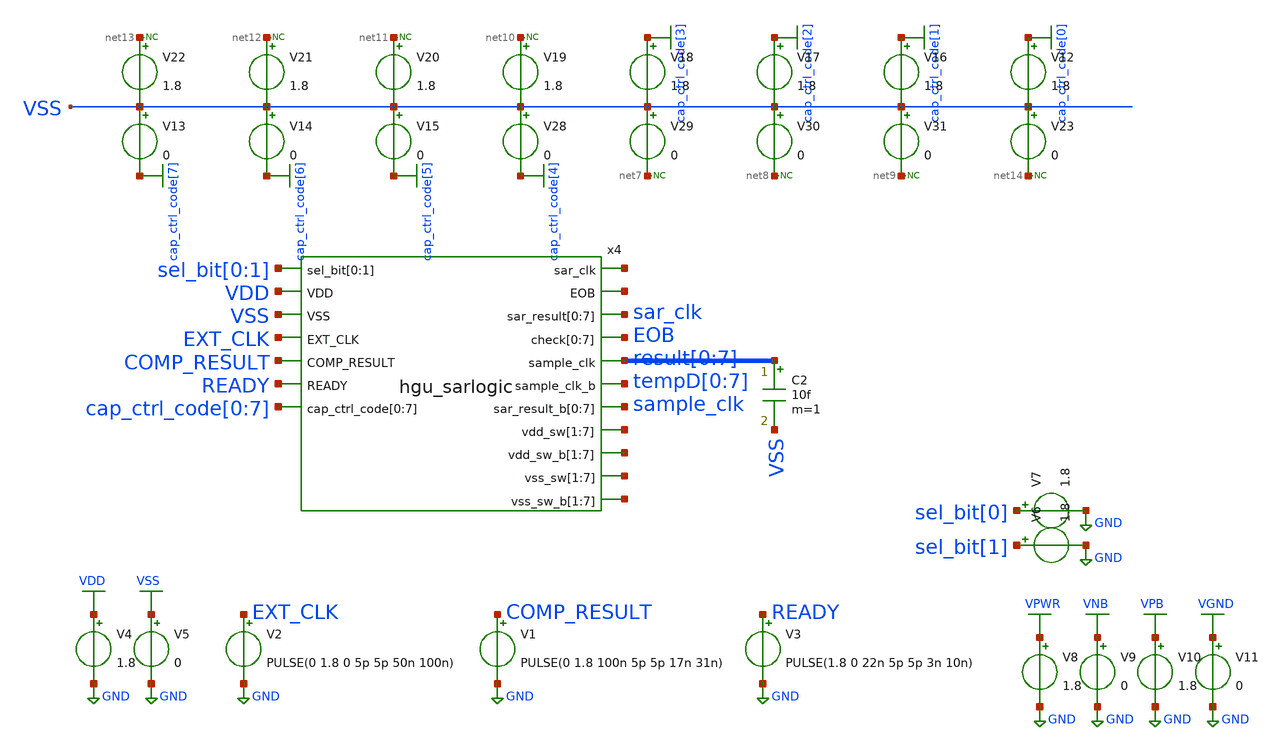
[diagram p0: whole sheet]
** sch_path: hgu/tb/tb_hgu_sarlogic_clk.sch
**.subckt tb_hgu_sarlogic_clk
V2 EXT_CLK GND PULSE(0 1.8 0 5p 5p 50n 100n)
V4 VDD GND 1.8
V1 COMP_RESULT GND PULSE(0 1.8 100n 5p 5p 17n 31n)
V5 VSS GND 0
V3 READY GND PULSE(1.8 0 22n 5p 5p 3n 10n)
x4 net1 net2 sar_clk sar_clk sar_clk sar_clk sar_clk sar_clk sar_clk sar_clk EOB EOB EOB EOB EOB EOB
+ EOB EOB result[0] sel_bit[0] sel_bit[1] tempD[0] VDD sample_clk sample_clk sample_clk sample_clk
+ sample_clk sample_clk sample_clk sample_clk VSS EXT_CLK COMP_RESULT READY net3[6] net3[5] net3[4] net3[3]
+ net3[2] net3[1] net3[0] net4[6] net4[5] net4[4] net4[3] net4[2] net4[1] net4[0] net5[6] net5[5] net5[4]
+ net5[3] net5[2] net5[1] net5[0] net6[6] net6[5] net6[4] net6[3] net6[2] net6[1] net6[0] cap_ctrl_code[0]
+ cap_ctrl_code[1] cap_ctrl_code[2] cap_ctrl_code[3] cap_ctrl_code[4] cap_ctrl_code[5] cap_ctrl_code[6]
+ cap_ctrl_code[7] hgu_sarlogic
C2 result[0] VSS 10f m=1
V6 sel_bit[1] GND 1.8
V7 sel_bit[0] GND 1.8
V8 VPWR GND 1.8
V9 VNB GND 0
V10 VPB GND 1.8
V11 VGND GND 0
V12 cap_ctrl_code[0] VSS 1.8
V13 VSS cap_ctrl_code[7] 0
V14 VSS cap_ctrl_code[6] 0
V15 VSS cap_ctrl_code[5] 0
V28 VSS cap_ctrl_code[4] 0
V29 VSS net7 0
V30 VSS net8 0
V31 VSS net9 0
V16 cap_ctrl_code[1] VSS 1.8
V17 cap_ctrl_code[2] VSS 1.8
V18 cap_ctrl_code[3] VSS 1.8
V19 net10 VSS 1.8
V20 net11 VSS 1.8
V21 net12 VSS 1.8
V22 net13 VSS 1.8
V23 VSS net14 0
* noconn #net13
* noconn #net12
* noconn #net11
* noconn #net10
* noconn #net7
* noconn #net8
* noconn #net9
* noconn #net14
**** begin user architecture code



.lib /foss/pdks/sky130A/libs.tech/ngspice/sky130.lib.spice tt
.include /foss/pdks/sky130A/libs.ref/sky130_fd_sc_hd/spice/sky130_fd_sc_hd.spice

.tran 10ps 400ns

.control
	option temp = 25
	let vdd_act = 1.8

	alter V4 vdd_act
	alter V8 vdd_act
	alter V10 vdd_act

	run
	plot V(EXT_CLK)-2 V(sample_clk) V(EOB)+2 V(READY)+4 V(sar_clk)+6 V(COMP_RESULT)+8
	plot V("tempD[0]") V("tempD[1]")+2 V("tempD[2]")+4 V("tempD[3]")+6 V("tempD[4]")+8 V("tempD[5]")+10
+ V("tempD[6]")+12 V("tempD[7]")+14 V(sar_clk) V(sar_clk)+2 V(sar_clk)+4 V(sar_clk)+6 V(sar_clk)+8 V(sar_clk)+10
+ V(sar_clk)+12 V(sar_clk)+14 V(EOB)-2
	plot V("result[0]") V("result[1]")+2 V("result[2]")+4 V("result[3]")+6 V("result[4]")+8
+ V("result[5]")+10 V("result[6]")+12 V("result[7]")+14
 .endc
.save all



**** end user architecture code
**.ends
.GLOBAL GND
.GLOBAL VDD
.GLOBAL VSS
.GLOBAL VGND
.GLOBAL VNB
.GLOBAL VPB
.GLOBAL VPWR
.GLOBAL cap_ctrl_code[7]
.GLOBAL cap_ctrl_code[6]
.GLOBAL cap_ctrl_code[5]
.GLOBAL cap_ctrl_code[4]
.GLOBAL cap_ctrl_code[3]
.GLOBAL cap_ctrl_code[2]
.GLOBAL cap_ctrl_code[1]
.GLOBAL cap_ctrl_code[0]
.end
